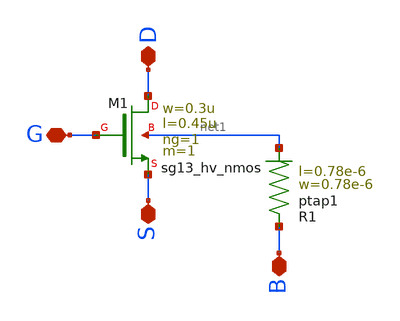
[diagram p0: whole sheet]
** sch_path: ihp-sg13cmos5l/schematic/xschem/sg13_hv_nmos_tap.sch
**.subckt sg13_hv_nmos_tap D S G B
*.iopin D
*.iopin S
*.iopin G
*.iopin B
XR1 B net1 ptap1 R=262.8 w=0.78e-6 l=0.78e-6
XM1 D G S net1 sg13_hv_nmos w=0.3u l=0.45u ng=1 m=1 mm_ok=1
**.ends
.end
